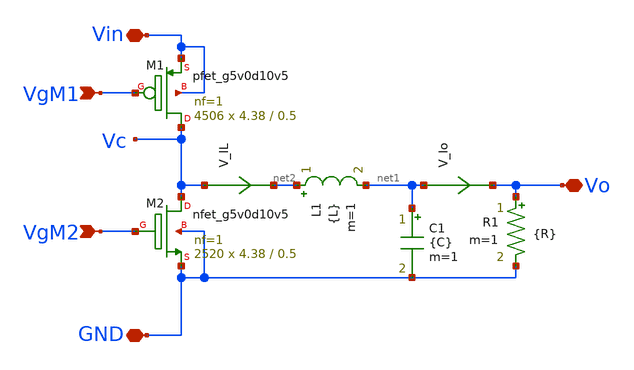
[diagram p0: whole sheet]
** sch_path: xschem/Modulos/DCDC_Buck.sch
**.subckt DCDC_Buck Vin VgM1 VgM2 Vo GND
*.iopin Vin
*.ipin VgM1
*.ipin VgM2
*.iopin Vo
*.iopin GND
L1 net2 net1 {L} m=1
C1 net1 GND {C} m=1
V_Io net1 Vo 0
.save i(v_io)
V_IL Vc net2 0
.save i(v_il)
R1 Vo GND {R} m=1
XM1 Vc VgM1 Vin Vin sky130_fd_pr__pfet_g5v0d10v5 L=0.5 W=4.38 nf=1 ad='int((nf+1)/2) * W/nf * 0.29' as='int((nf+2)/2) * W/nf * 0.29'
+ pd='2*int((nf+1)/2) * (W/nf + 0.29)' ps='2*int((nf+2)/2) * (W/nf + 0.29)' nrd='0.29 / W' nrs='0.29 / W'
+ sa=0 sb=0 sd=0 mult=4506 m=4506
XM2 Vc VgM2 GND GND sky130_fd_pr__nfet_g5v0d10v5 L=0.5 W=4.38 nf=1 ad='int((nf+1)/2) * W/nf * 0.29' as='int((nf+2)/2) * W/nf * 0.29'
+ pd='2*int((nf+1)/2) * (W/nf + 0.29)' ps='2*int((nf+2)/2) * (W/nf + 0.29)' nrd='0.29 / W' nrs='0.29 / W'
+ sa=0 sb=0 sd=0 mult=2520 m=2520
**.ends
.end
